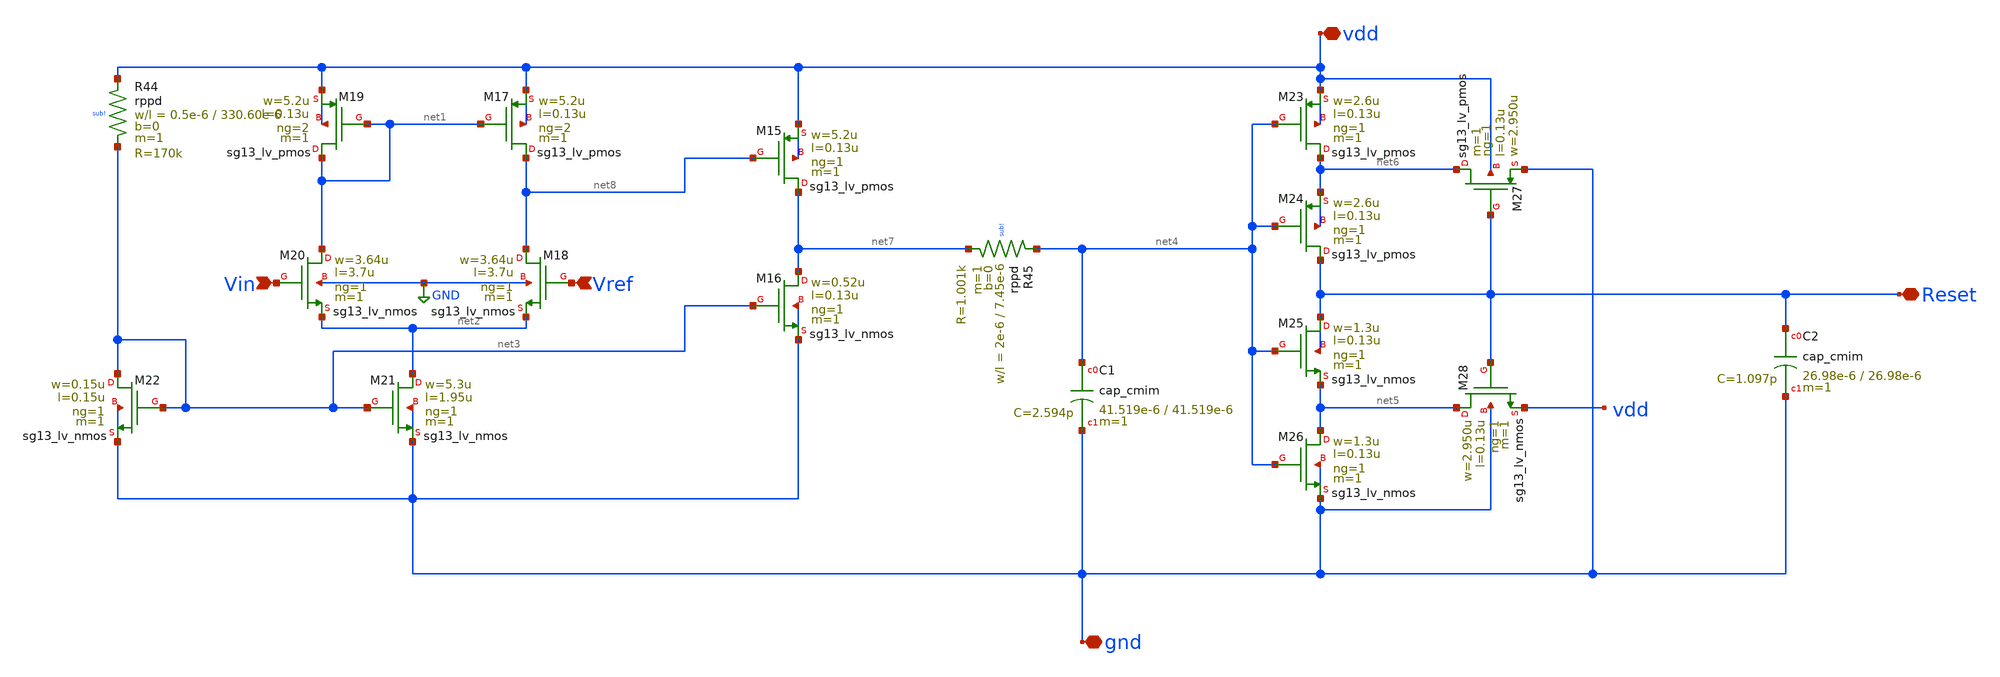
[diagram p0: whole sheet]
** sch_path: dependencies/POR/POR-main/testbenches/tran_mc/xschem/POR_symbol.sch
**.subckt POR_symbol vdd gnd Vin Vref Reset
*.iopin vdd
*.iopin gnd
*.ipin Vin
*.ipin Vref
*.iopin Reset
XM15 net7 net8 vdd vdd sg13_lv_pmos w=5.2u l=0.13u ng=1 m=1 mm_ok=1
XM16 net7 net3 gnd gnd sg13_lv_nmos w=0.52u l=0.13u ng=1 m=1 mm_ok=1
XM17 net8 net1 vdd vdd sg13_lv_pmos w=5.2u l=0.13u ng=2 m=1 mm_ok=1
XM18 net8 Vref net2 GND sg13_lv_nmos w=3.64u l=3.7u ng=1 m=1 mm_ok=1
XM19 net1 net1 vdd vdd sg13_lv_pmos w=5.2u l=0.13u ng=2 m=1 mm_ok=1
XM20 net1 Vin net2 GND sg13_lv_nmos w=3.64u l=3.7u ng=1 m=1 mm_ok=1
XM21 net2 net3 gnd gnd sg13_lv_nmos w=5.3u l=1.95u ng=1 m=1 mm_ok=1
XM22 net3 net3 gnd gnd sg13_lv_nmos w=0.15u l=0.15u ng=1 m=1 mm_ok=1
XM23 net6 net4 vdd vdd sg13_lv_pmos w=2.6u l=0.13u ng=1 m=1 mm_ok=1
XM24 Reset net4 net6 net6 sg13_lv_pmos w=2.6u l=0.13u ng=1 m=1 mm_ok=1
XM25 Reset net4 net5 Reset sg13_lv_nmos w=1.3u l=0.13u ng=1 m=1 mm_ok=1
XM26 net5 net4 gnd gnd sg13_lv_nmos w=1.3u l=0.13u ng=1 m=1 mm_ok=1
XM27 net6 Reset gnd vdd sg13_lv_pmos w=2.950u l=0.13u ng=1 m=1 mm_ok=1
XM28 net5 Reset vdd gnd sg13_lv_nmos w=2.950u l=0.13u ng=1 m=1 mm_ok=1
XR44 vdd net3 sub! rppd w=0.5e-6 l=330.60e-6 m=1 b=0 mm_ok=1
XC2 Reset gnd cap_cmim w=26.98e-6 l=26.98e-6 m=1 mm_ok=1
XC1 net4 gnd cap_cmim w=41.519e-6 l=41.519e-6 m=1 mm_ok=1
XR45 net4 net7 sub! rppd w=2e-6 l=7.45e-6 m=1 b=0 mm_ok=1
**.ends
.GLOBAL GND
.end
